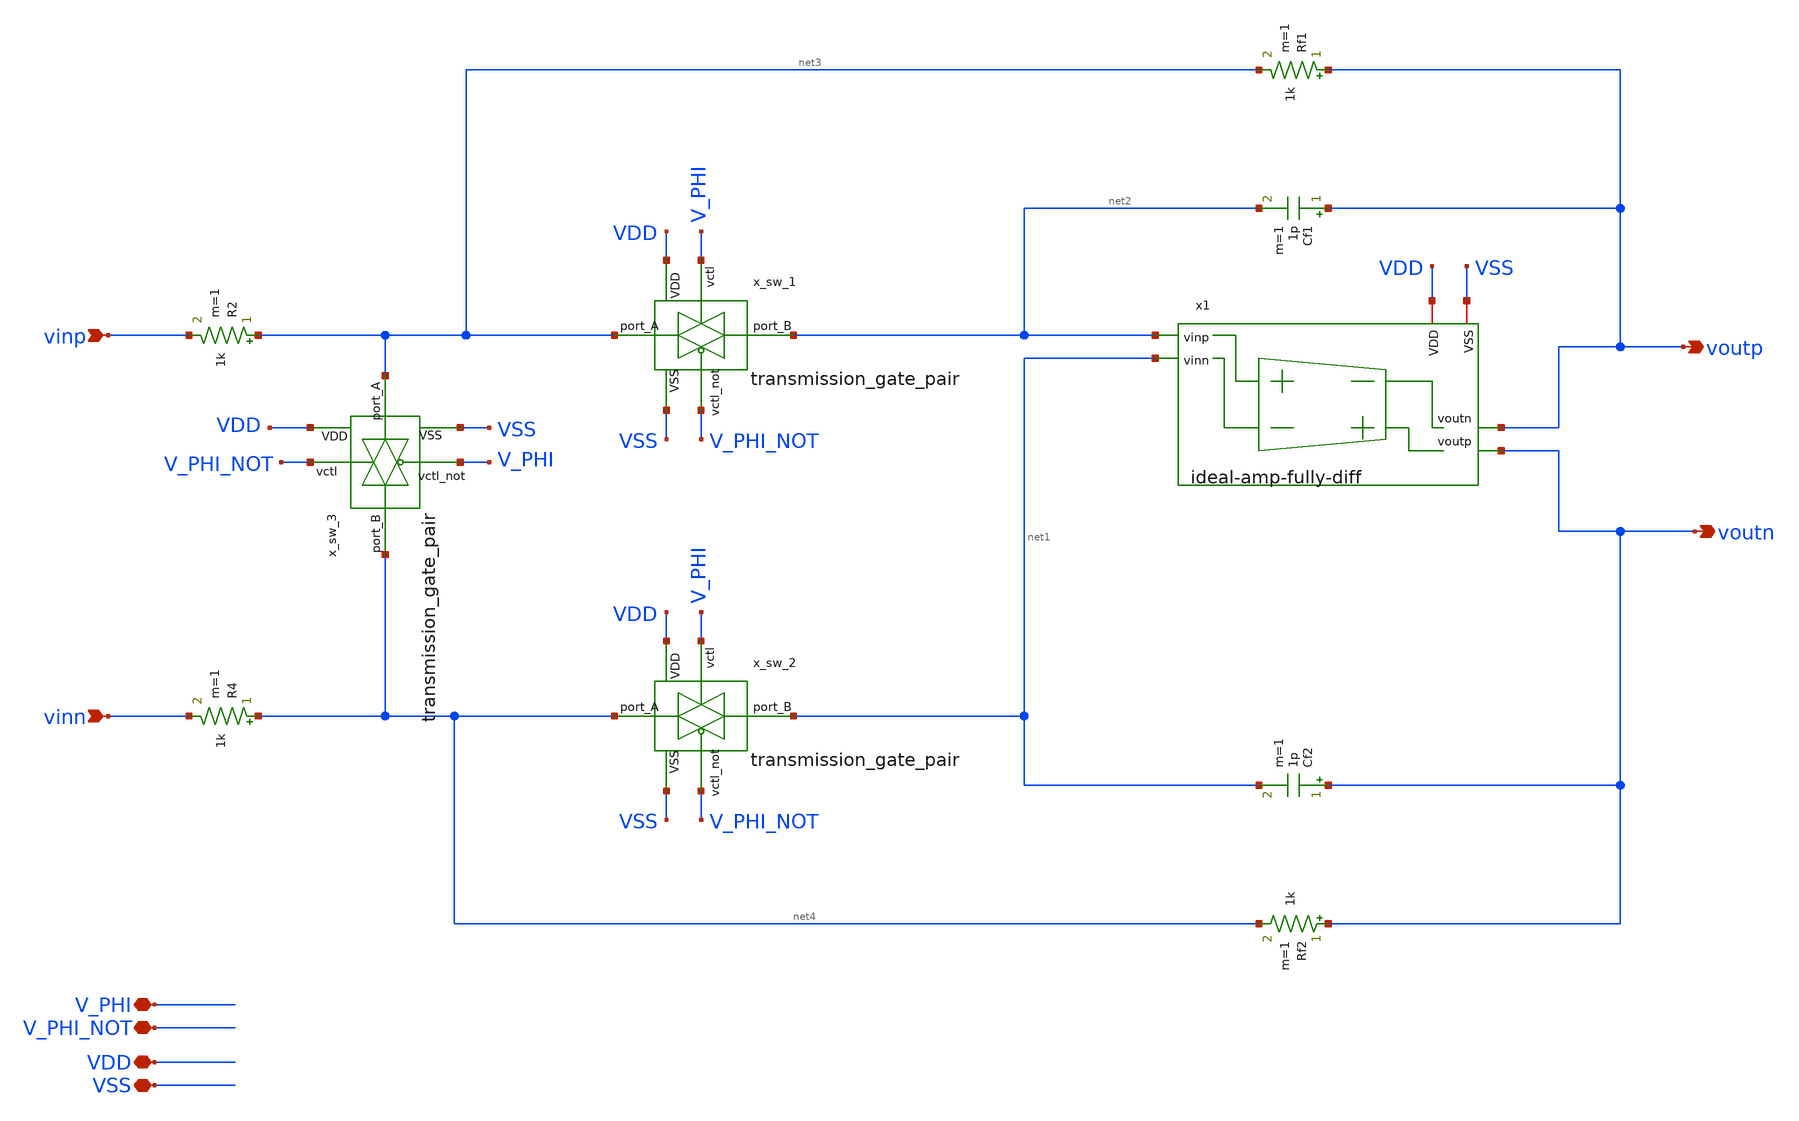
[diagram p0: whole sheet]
** sch_path: analog-db/drawings/bio-afe-01-YuPinHsu-reconfigable-SRMC/SRMC-ideal.sch
* Copyright 2026 MacAnalog Research Group
**.subckt SRMC-ideal V_PHI V_PHI_NOT vinp vinn voutn voutp VDD VSS
*.iopin V_PHI
*.iopin V_PHI_NOT
*.ipin vinp
*.ipin vinn
*.opin voutn
*.opin voutp
*.iopin VDD
*.iopin VSS
x1 net2 net1 voutp voutn VSS VDD ideal-amp-fully-diff
Rf1 voutp net3 1k m=1
Cf1 voutp net2 1p m=1
Rf2 voutn net4 1k m=1
Cf2 voutn net1 1p m=1
R2 net3 vinp 1k m=1
R4 net4 vinn 1k m=1
x_sw_1 V_PHI_NOT VDD net2 VSS net3 V_PHI transmission_gate_pair
x_sw_2 V_PHI_NOT VDD net1 VSS net4 V_PHI transmission_gate_pair
x_sw_3 V_PHI VDD net4 VSS net3 V_PHI_NOT transmission_gate_pair
**.ends

* expanding   symbol:  shared/ideal/ideal-amp-fully-diff.sym # of pins=6
** sym_path: analog-db/circuits/amp_028_ideal_fully_diff/pdk/ihp-sg13g2/schematic/ideal-amp-fully-diff.sym
** sch_path: analog-db/circuits/amp_028_ideal_fully_diff/pdk/ihp-sg13g2/schematic/ideal-amp-fully-diff.sch
.subckt ideal-amp-fully-diff vinp vinn voutn voutp VSS VDD
*.ipin vinp
*.ipin vinn
*.opin voutp
*.opin voutn
*.iopin VDD
*.iopin VSS
Gm voutn voutp vinp vinn gm_val
Rout voutn voutp rout_val m=1
Rin vinp vinn rin_val m=1
Cout voutn voutp cout_val m=1
Cin vinp vinn cin_val m=1
* noconn VDD
* noconn VSS
.ends


* expanding   symbol:  shared/transmission_gate_pair.sym # of pins=6
** sym_path: analog-db/drawings/shared/transmission_gate_pair.sym
** sch_path: analog-db/drawings/shared/transmission_gate_pair.sch
.subckt transmission_gate_pair vctl_not VDD port_B VSS port_A vctl
*.ipin port_A
*.ipin port_B
*.ipin vctl
*.ipin VSS
*.ipin VDD
*.ipin vctl_not
XM1 port_A vctl port_B VSS sg13_lv_nmos w=tg_n_w l=tg_n_l ng=1 m=1 mm_ok=1
XM2 port_B vctl_not port_A VDD sg13_lv_pmos w=tg_p_w l=tg_p_l ng=1 m=1 mm_ok=1
.ends

.end
